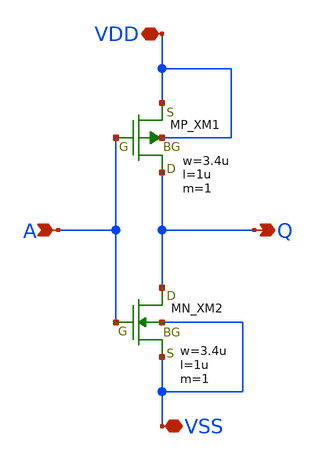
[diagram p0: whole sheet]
** sch_path: member_project/inverter/ZEP/Yourein/inverter_Yourein.sch
**.subckt inverter_Yourein A VSS Q VDD
*.ipin A
*.iopin VSS
*.opin Q
*.iopin VDD
XM1 Q A VDD VDD PMOS w=3.4u l=1u as=0 ad=0 ps=0 pd=0 nrd=0 nrs=0 m=1
XM2 Q A VSS VSS NMOS w=3.4u l=1u as=0 ad=0 ps=0 pd=0 nrd=0 nrs=0 m=1
**.ends
.end
